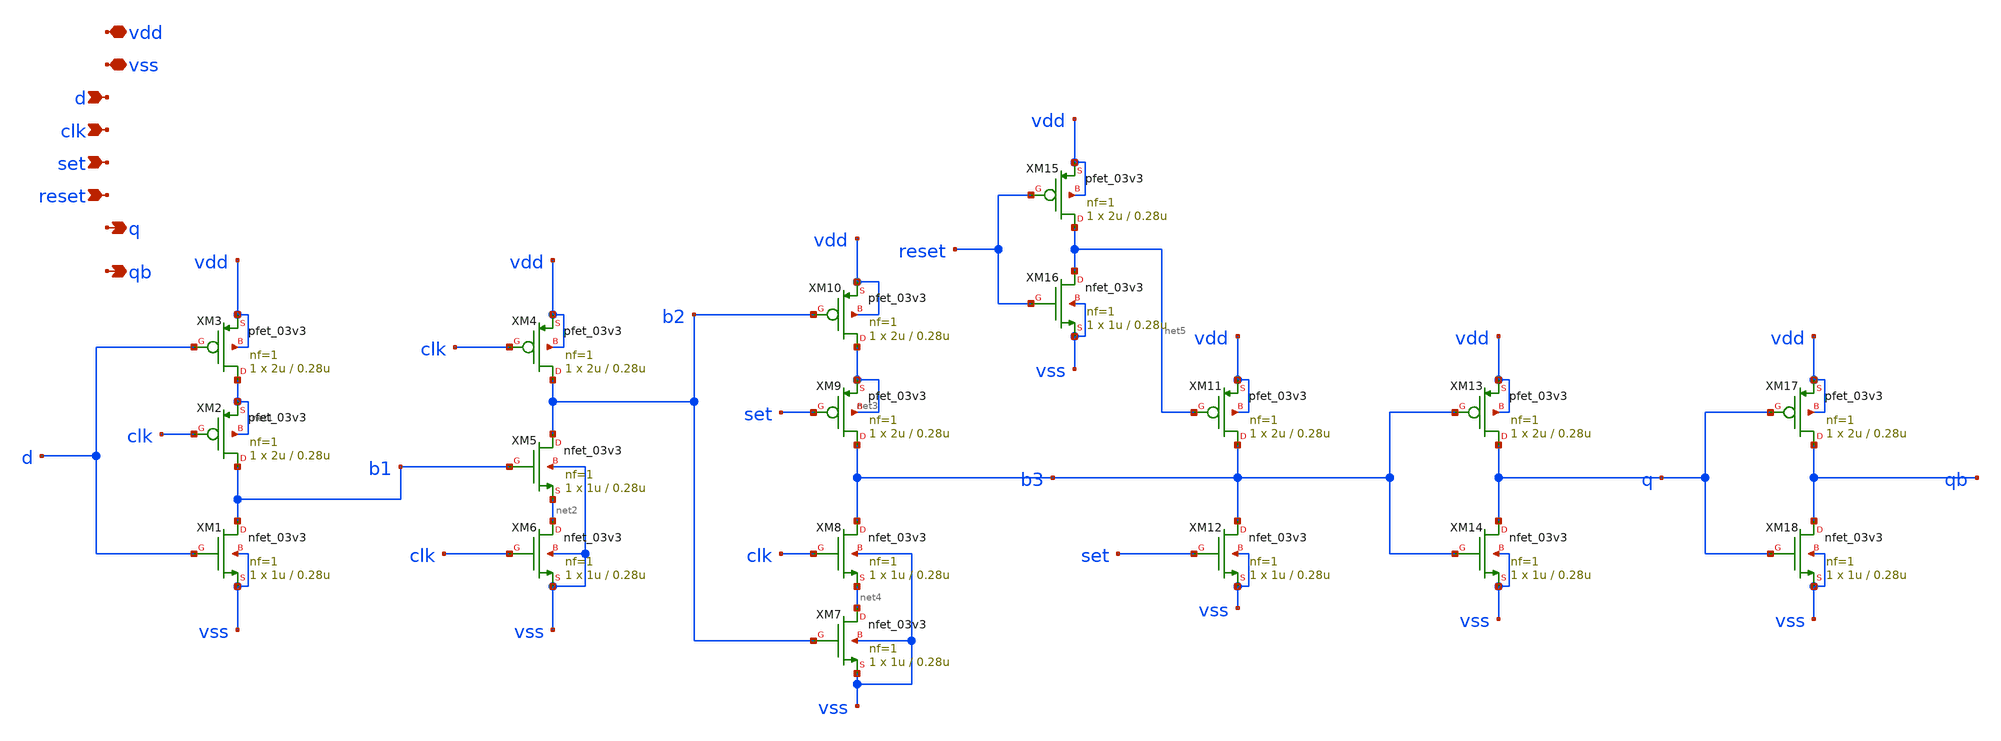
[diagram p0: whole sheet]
** sch_path: designs/libs/tspc_flip_flop/tspc_flip_flop.sch
**.subckt tspc_flip_flop vdd vss d clk set reset q qb
*.iopin vdd
*.iopin vss
*.ipin d
*.ipin clk
*.ipin set
*.ipin reset
*.opin q
*.opin qb
XM1 b1 d vss vss nfet_03v3 L=0.28u W=1u nf=1 ad='int((nf+1)/2) * W/nf * 0.18u' as='int((nf+2)/2) * W/nf * 0.18u'
+ pd='2*int((nf+1)/2) * (W/nf + 0.18u)' ps='2*int((nf+2)/2) * (W/nf + 0.18u)' nrd='0.18u / W' nrs='0.18u / W'
+ sa=0 sb=0 sd=0 m=1
XM2 b1 clk net1 net1 pfet_03v3 L=0.28u W=2u nf=1 ad='int((nf+1)/2) * W/nf * 0.18u' as='int((nf+2)/2) * W/nf * 0.18u'
+ pd='2*int((nf+1)/2) * (W/nf + 0.18u)' ps='2*int((nf+2)/2) * (W/nf + 0.18u)' nrd='0.18u / W' nrs='0.18u / W'
+ sa=0 sb=0 sd=0 m=1
XM3 net1 d vdd vdd pfet_03v3 L=0.28u W=2u nf=1 ad='int((nf+1)/2) * W/nf * 0.18u' as='int((nf+2)/2) * W/nf * 0.18u'
+ pd='2*int((nf+1)/2) * (W/nf + 0.18u)' ps='2*int((nf+2)/2) * (W/nf + 0.18u)' nrd='0.18u / W' nrs='0.18u / W'
+ sa=0 sb=0 sd=0 m=1
XM4 b2 clk vdd vdd pfet_03v3 L=0.28u W=2u nf=1 ad='int((nf+1)/2) * W/nf * 0.18u' as='int((nf+2)/2) * W/nf * 0.18u'
+ pd='2*int((nf+1)/2) * (W/nf + 0.18u)' ps='2*int((nf+2)/2) * (W/nf + 0.18u)' nrd='0.18u / W' nrs='0.18u / W'
+ sa=0 sb=0 sd=0 m=1
XM5 b2 b1 net2 vss nfet_03v3 L=0.28u W=1u nf=1 ad='int((nf+1)/2) * W/nf * 0.18u' as='int((nf+2)/2) * W/nf * 0.18u'
+ pd='2*int((nf+1)/2) * (W/nf + 0.18u)' ps='2*int((nf+2)/2) * (W/nf + 0.18u)' nrd='0.18u / W' nrs='0.18u / W'
+ sa=0 sb=0 sd=0 m=1
XM6 net2 clk vss vss nfet_03v3 L=0.28u W=1u nf=1 ad='int((nf+1)/2) * W/nf * 0.18u' as='int((nf+2)/2) * W/nf * 0.18u'
+ pd='2*int((nf+1)/2) * (W/nf + 0.18u)' ps='2*int((nf+2)/2) * (W/nf + 0.18u)' nrd='0.18u / W' nrs='0.18u / W'
+ sa=0 sb=0 sd=0 m=1
XM7 net4 b2 vss vss nfet_03v3 L=0.28u W=1u nf=1 ad='int((nf+1)/2) * W/nf * 0.18u' as='int((nf+2)/2) * W/nf * 0.18u'
+ pd='2*int((nf+1)/2) * (W/nf + 0.18u)' ps='2*int((nf+2)/2) * (W/nf + 0.18u)' nrd='0.18u / W' nrs='0.18u / W'
+ sa=0 sb=0 sd=0 m=1
XM8 b3 clk net4 vss nfet_03v3 L=0.28u W=1u nf=1 ad='int((nf+1)/2) * W/nf * 0.18u' as='int((nf+2)/2) * W/nf * 0.18u'
+ pd='2*int((nf+1)/2) * (W/nf + 0.18u)' ps='2*int((nf+2)/2) * (W/nf + 0.18u)' nrd='0.18u / W' nrs='0.18u / W'
+ sa=0 sb=0 sd=0 m=1
XM9 b3 set net3 net3 pfet_03v3 L=0.28u W=2u nf=1 ad='int((nf+1)/2) * W/nf * 0.18u' as='int((nf+2)/2) * W/nf * 0.18u'
+ pd='2*int((nf+1)/2) * (W/nf + 0.18u)' ps='2*int((nf+2)/2) * (W/nf + 0.18u)' nrd='0.18u / W' nrs='0.18u / W'
+ sa=0 sb=0 sd=0 m=1
XM10 net3 b2 vdd vdd pfet_03v3 L=0.28u W=2u nf=1 ad='int((nf+1)/2) * W/nf * 0.18u' as='int((nf+2)/2) * W/nf * 0.18u'
+ pd='2*int((nf+1)/2) * (W/nf + 0.18u)' ps='2*int((nf+2)/2) * (W/nf + 0.18u)' nrd='0.18u / W' nrs='0.18u / W'
+ sa=0 sb=0 sd=0 m=1
XM11 b3 net5 vdd vdd pfet_03v3 L=0.28u W=2u nf=1 ad='int((nf+1)/2) * W/nf * 0.18u' as='int((nf+2)/2) * W/nf * 0.18u'
+ pd='2*int((nf+1)/2) * (W/nf + 0.18u)' ps='2*int((nf+2)/2) * (W/nf + 0.18u)' nrd='0.18u / W' nrs='0.18u / W'
+ sa=0 sb=0 sd=0 m=1
XM12 b3 set vss vss nfet_03v3 L=0.28u W=1u nf=1 ad='int((nf+1)/2) * W/nf * 0.18u' as='int((nf+2)/2) * W/nf * 0.18u'
+ pd='2*int((nf+1)/2) * (W/nf + 0.18u)' ps='2*int((nf+2)/2) * (W/nf + 0.18u)' nrd='0.18u / W' nrs='0.18u / W'
+ sa=0 sb=0 sd=0 m=1
XM13 q b3 vdd vdd pfet_03v3 L=0.28u W=2u nf=1 ad='int((nf+1)/2) * W/nf * 0.18u' as='int((nf+2)/2) * W/nf * 0.18u'
+ pd='2*int((nf+1)/2) * (W/nf + 0.18u)' ps='2*int((nf+2)/2) * (W/nf + 0.18u)' nrd='0.18u / W' nrs='0.18u / W'
+ sa=0 sb=0 sd=0 m=1
XM14 q b3 vss vss nfet_03v3 L=0.28u W=1u nf=1 ad='int((nf+1)/2) * W/nf * 0.18u' as='int((nf+2)/2) * W/nf * 0.18u'
+ pd='2*int((nf+1)/2) * (W/nf + 0.18u)' ps='2*int((nf+2)/2) * (W/nf + 0.18u)' nrd='0.18u / W' nrs='0.18u / W'
+ sa=0 sb=0 sd=0 m=1
XM15 net5 reset vdd vdd pfet_03v3 L=0.28u W=2u nf=1 ad='int((nf+1)/2) * W/nf * 0.18u' as='int((nf+2)/2) * W/nf * 0.18u'
+ pd='2*int((nf+1)/2) * (W/nf + 0.18u)' ps='2*int((nf+2)/2) * (W/nf + 0.18u)' nrd='0.18u / W' nrs='0.18u / W'
+ sa=0 sb=0 sd=0 m=1
XM16 net5 reset vss vss nfet_03v3 L=0.28u W=1u nf=1 ad='int((nf+1)/2) * W/nf * 0.18u' as='int((nf+2)/2) * W/nf * 0.18u'
+ pd='2*int((nf+1)/2) * (W/nf + 0.18u)' ps='2*int((nf+2)/2) * (W/nf + 0.18u)' nrd='0.18u / W' nrs='0.18u / W'
+ sa=0 sb=0 sd=0 m=1
XM17 qb q vdd vdd pfet_03v3 L=0.28u W=2u nf=1 ad='int((nf+1)/2) * W/nf * 0.18u' as='int((nf+2)/2) * W/nf * 0.18u'
+ pd='2*int((nf+1)/2) * (W/nf + 0.18u)' ps='2*int((nf+2)/2) * (W/nf + 0.18u)' nrd='0.18u / W' nrs='0.18u / W'
+ sa=0 sb=0 sd=0 m=1
XM18 qb q vss vss nfet_03v3 L=0.28u W=1u nf=1 ad='int((nf+1)/2) * W/nf * 0.18u' as='int((nf+2)/2) * W/nf * 0.18u'
+ pd='2*int((nf+1)/2) * (W/nf + 0.18u)' ps='2*int((nf+2)/2) * (W/nf + 0.18u)' nrd='0.18u / W' nrs='0.18u / W'
+ sa=0 sb=0 sd=0 m=1
**.ends
.end
